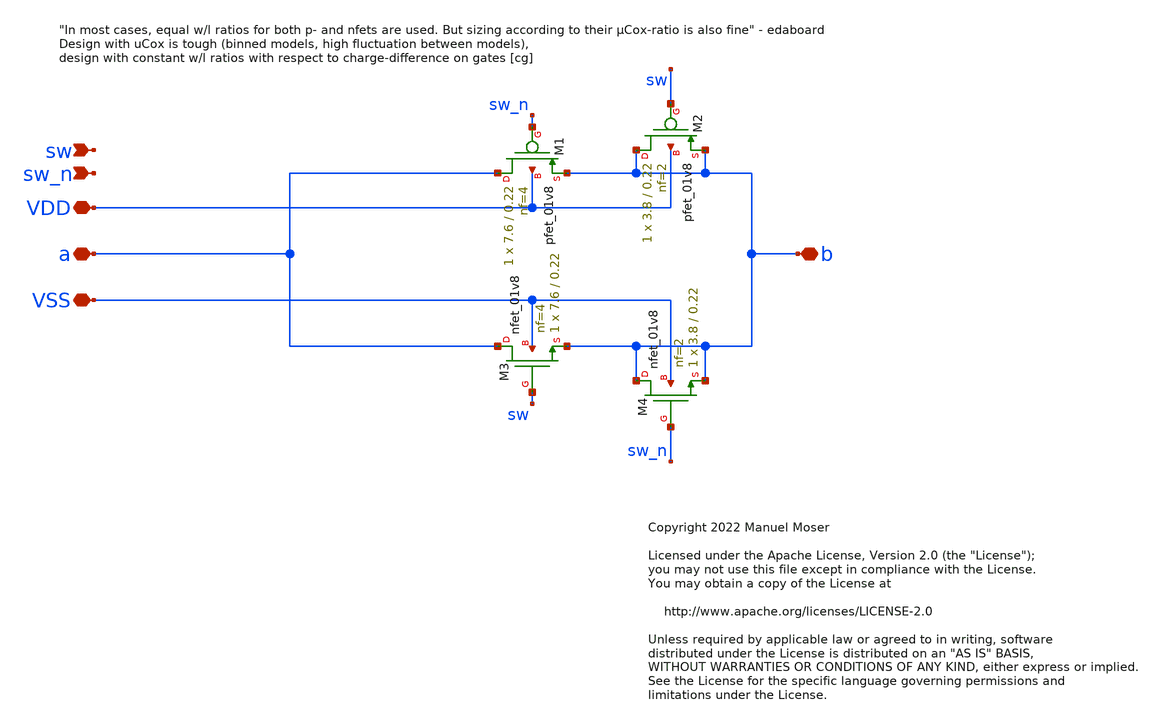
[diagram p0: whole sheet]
** sch_path: xschem/adc_gate_switch.sch
* Copyright 2022 Manuel Moser
* Licensed under the Apache License, Version 2.0 (the "License");
**.subckt adc_gate_switch VSS VDD sw_n sw a b
*.iopin VSS
*.iopin VDD
*.ipin sw_n
*.ipin sw
*.iopin a
*.iopin b
XM1 a sw_n b VDD sky130_fd_pr__pfet_01v8 L=0.22 W=7.6 nf=4 ad='int((nf+1)/2) * W/nf * 0.29' as='int((nf+2)/2) * W/nf * 0.29'
+ pd='2*int((nf+1)/2) * (W/nf + 0.29)' ps='2*int((nf+2)/2) * (W/nf + 0.29)' nrd='0.29 / W' nrs='0.29 / W'
+ sa=0 sb=0 sd=0 mult=1 m=1
XM3 a sw b VSS sky130_fd_pr__nfet_01v8 L=0.22 W=7.6 nf=4 ad='int((nf+1)/2) * W/nf * 0.29' as='int((nf+2)/2) * W/nf * 0.29'
+ pd='2*int((nf+1)/2) * (W/nf + 0.29)' ps='2*int((nf+2)/2) * (W/nf + 0.29)' nrd='0.29 / W' nrs='0.29 / W'
+ sa=0 sb=0 sd=0 mult=1 m=1
XM2 b sw b VDD sky130_fd_pr__pfet_01v8 L=0.22 W=3.8 nf=2 ad='int((nf+1)/2) * W/nf * 0.29' as='int((nf+2)/2) * W/nf * 0.29'
+ pd='2*int((nf+1)/2) * (W/nf + 0.29)' ps='2*int((nf+2)/2) * (W/nf + 0.29)' nrd='0.29 / W' nrs='0.29 / W'
+ sa=0 sb=0 sd=0 mult=1 m=1
XM4 b sw_n b VSS sky130_fd_pr__nfet_01v8 L=0.22 W=3.8 nf=2 ad='int((nf+1)/2) * W/nf * 0.29' as='int((nf+2)/2) * W/nf * 0.29'
+ pd='2*int((nf+1)/2) * (W/nf + 0.29)' ps='2*int((nf+2)/2) * (W/nf + 0.29)' nrd='0.29 / W' nrs='0.29 / W'
+ sa=0 sb=0 sd=0 mult=1 m=1
**.ends
.end
